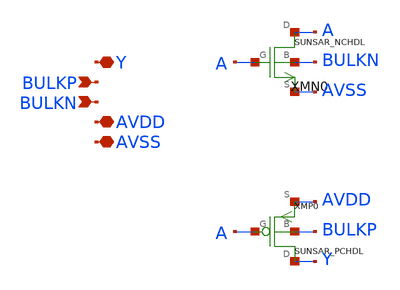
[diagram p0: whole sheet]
** sch_path: ip/sun_sar9b_sky130nm/design/SUN_SAR9B_SKY130NM/SUNSAR_TIEH_CV.sch
**.subckt SUNSAR_TIEH_CV Y BULKP BULKN AVDD AVSS
*.iopin Y
*.ipin BULKP
*.ipin BULKN
*.iopin AVDD
*.iopin AVSS
XMN0 A A AVSS BULKN SUNSAR_NCHDL
XMP0 Y A AVDD BULKP SUNSAR_PCHDL
**.ends
.end
